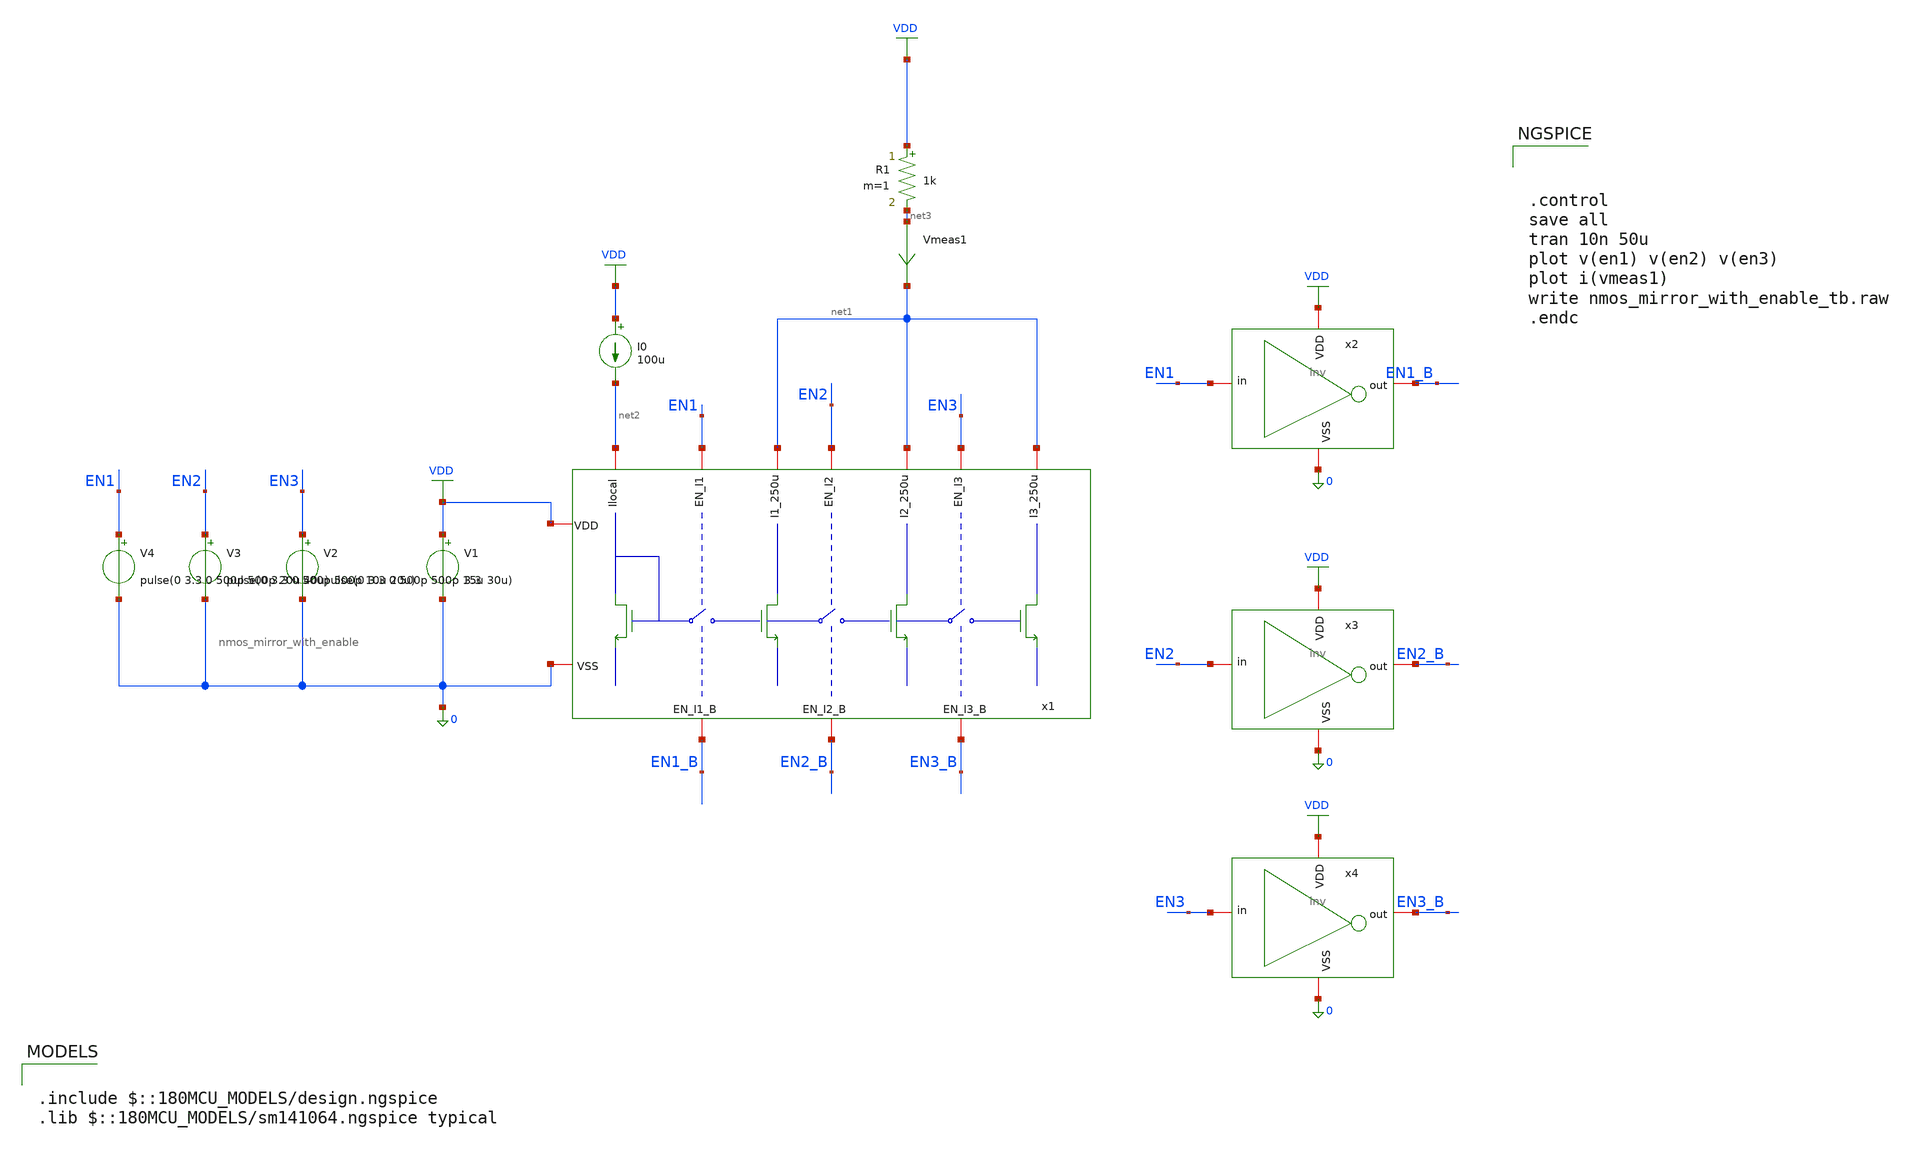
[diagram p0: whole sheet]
** sch_path: designs/mirrors/testbench/nmos_mirror_with_enable_tb.sch
**.subckt nmos_mirror_with_enable_tb
x1 EN3 net1 EN3_B EN2 net1 EN2_B net2 VDD EN1 net1 0 EN1_B nmos_mirror_with_enable
V1 VDD 0 3.3
x2 VDD EN1_B EN1 0 inv
x3 VDD EN2_B EN2 0 inv
x4 VDD EN3_B EN3 0 inv
Vmeas1 net3 net1 0
.save i(vmeas1)
V2 EN3 0 pulse(0 3.3 0 500p 500p 15u 30u)
V3 EN2 0 pulse(0 3.3 0 500p 500p 10u 20u)
V4 EN1 0 pulse(0 3.3 0 500p 500p 20u 40u)
I0 VDD net2 100u
R1 VDD net3 1k m=1
**** begin user architecture code

.include $::180MCU_MODELS/design.ngspice
.lib $::180MCU_MODELS/sm141064.ngspice typical




.control
save all
tran 10n 50u
plot v(en1) v(en2) v(en3)
plot i(vmeas1)
write nmos_mirror_with_enable_tb.raw
.endc


**** end user architecture code
**.ends
.GLOBAL VDD
.end
